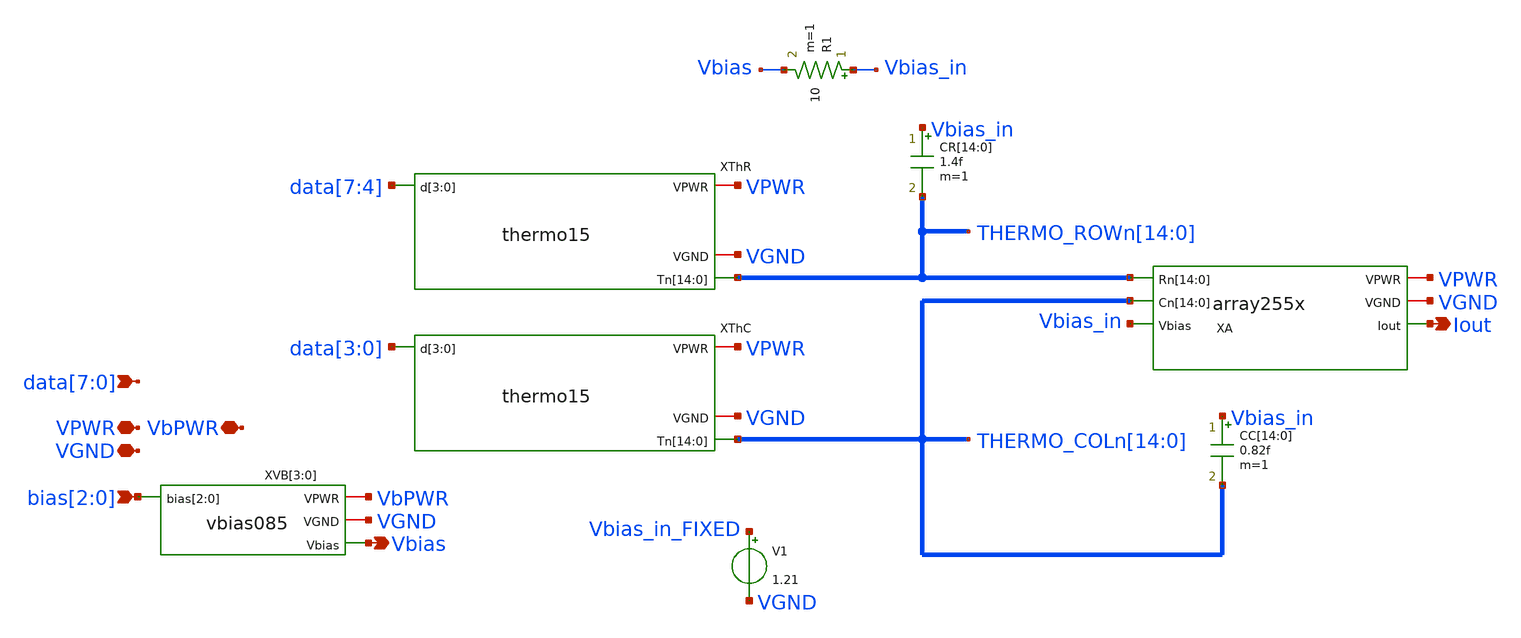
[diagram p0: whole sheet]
** sch_path: xschem/csdac255.sch
**.subckt csdac255 VPWR Iout VGND bias[2],bias[1],bias[0]
*+ data[7],data[6],data[5],data[4],data[3],data[2],data[1],data[0] VbPWR Vbias
*.iopin VPWR
*.opin Iout
*.iopin VGND
*.ipin bias[2],bias[1],bias[0]
*.ipin data[7],data[6],data[5],data[4],data[3],data[2],data[1],data[0]
*.iopin VbPWR
*.opin Vbias
XThR VPWR VGND THERMO_ROWn[14] THERMO_ROWn[13] THERMO_ROWn[12] THERMO_ROWn[11] THERMO_ROWn[10]
+ THERMO_ROWn[9] THERMO_ROWn[8] THERMO_ROWn[7] THERMO_ROWn[6] THERMO_ROWn[5] THERMO_ROWn[4] THERMO_ROWn[3]
+ THERMO_ROWn[2] THERMO_ROWn[1] THERMO_ROWn[0] data[7] data[6] data[5] data[4] thermo15
XA VPWR VGND THERMO_ROWn[14] THERMO_ROWn[13] THERMO_ROWn[12] THERMO_ROWn[11] THERMO_ROWn[10]
+ THERMO_ROWn[9] THERMO_ROWn[8] THERMO_ROWn[7] THERMO_ROWn[6] THERMO_ROWn[5] THERMO_ROWn[4] THERMO_ROWn[3]
+ THERMO_ROWn[2] THERMO_ROWn[1] THERMO_ROWn[0] THERMO_COLn[14] THERMO_COLn[13] THERMO_COLn[12] THERMO_COLn[11]
+ THERMO_COLn[10] THERMO_COLn[9] THERMO_COLn[8] THERMO_COLn[7] THERMO_COLn[6] THERMO_COLn[5] THERMO_COLn[4]
+ THERMO_COLn[3] THERMO_COLn[2] THERMO_COLn[1] THERMO_COLn[0] Vbias_in Iout array255x
XThC VPWR VGND THERMO_COLn[14] THERMO_COLn[13] THERMO_COLn[12] THERMO_COLn[11] THERMO_COLn[10]
+ THERMO_COLn[9] THERMO_COLn[8] THERMO_COLn[7] THERMO_COLn[6] THERMO_COLn[5] THERMO_COLn[4] THERMO_COLn[3]
+ THERMO_COLn[2] THERMO_COLn[1] THERMO_COLn[0] data[3] data[2] data[1] data[0] thermo15
CR[14] Vbias_in THERMO_ROWn[14] 1.4f m=1
CR[13] Vbias_in THERMO_ROWn[13] 1.4f m=1
CR[12] Vbias_in THERMO_ROWn[12] 1.4f m=1
CR[11] Vbias_in THERMO_ROWn[11] 1.4f m=1
CR[10] Vbias_in THERMO_ROWn[10] 1.4f m=1
CR[9] Vbias_in THERMO_ROWn[9] 1.4f m=1
CR[8] Vbias_in THERMO_ROWn[8] 1.4f m=1
CR[7] Vbias_in THERMO_ROWn[7] 1.4f m=1
CR[6] Vbias_in THERMO_ROWn[6] 1.4f m=1
CR[5] Vbias_in THERMO_ROWn[5] 1.4f m=1
CR[4] Vbias_in THERMO_ROWn[4] 1.4f m=1
CR[3] Vbias_in THERMO_ROWn[3] 1.4f m=1
CR[2] Vbias_in THERMO_ROWn[2] 1.4f m=1
CR[1] Vbias_in THERMO_ROWn[1] 1.4f m=1
CR[0] Vbias_in THERMO_ROWn[0] 1.4f m=1
CC[14] Vbias_in THERMO_COLn[14] 0.82f m=1
CC[13] Vbias_in THERMO_COLn[13] 0.82f m=1
CC[12] Vbias_in THERMO_COLn[12] 0.82f m=1
CC[11] Vbias_in THERMO_COLn[11] 0.82f m=1
CC[10] Vbias_in THERMO_COLn[10] 0.82f m=1
CC[9] Vbias_in THERMO_COLn[9] 0.82f m=1
CC[8] Vbias_in THERMO_COLn[8] 0.82f m=1
CC[7] Vbias_in THERMO_COLn[7] 0.82f m=1
CC[6] Vbias_in THERMO_COLn[6] 0.82f m=1
CC[5] Vbias_in THERMO_COLn[5] 0.82f m=1
CC[4] Vbias_in THERMO_COLn[4] 0.82f m=1
CC[3] Vbias_in THERMO_COLn[3] 0.82f m=1
CC[2] Vbias_in THERMO_COLn[2] 0.82f m=1
CC[1] Vbias_in THERMO_COLn[1] 0.82f m=1
CC[0] Vbias_in THERMO_COLn[0] 0.82f m=1
XVB[3] VbPWR VGND bias[2] bias[1] bias[0] Vbias vbias085
XVB[2] VbPWR VGND bias[2] bias[1] bias[0] Vbias vbias085
XVB[1] VbPWR VGND bias[2] bias[1] bias[0] Vbias vbias085
XVB[0] VbPWR VGND bias[2] bias[1] bias[0] Vbias vbias085
R1 Vbias_in Vbias 10 m=1
V1 Vbias_in_FIXED VGND 1.21
**.ends
.end
